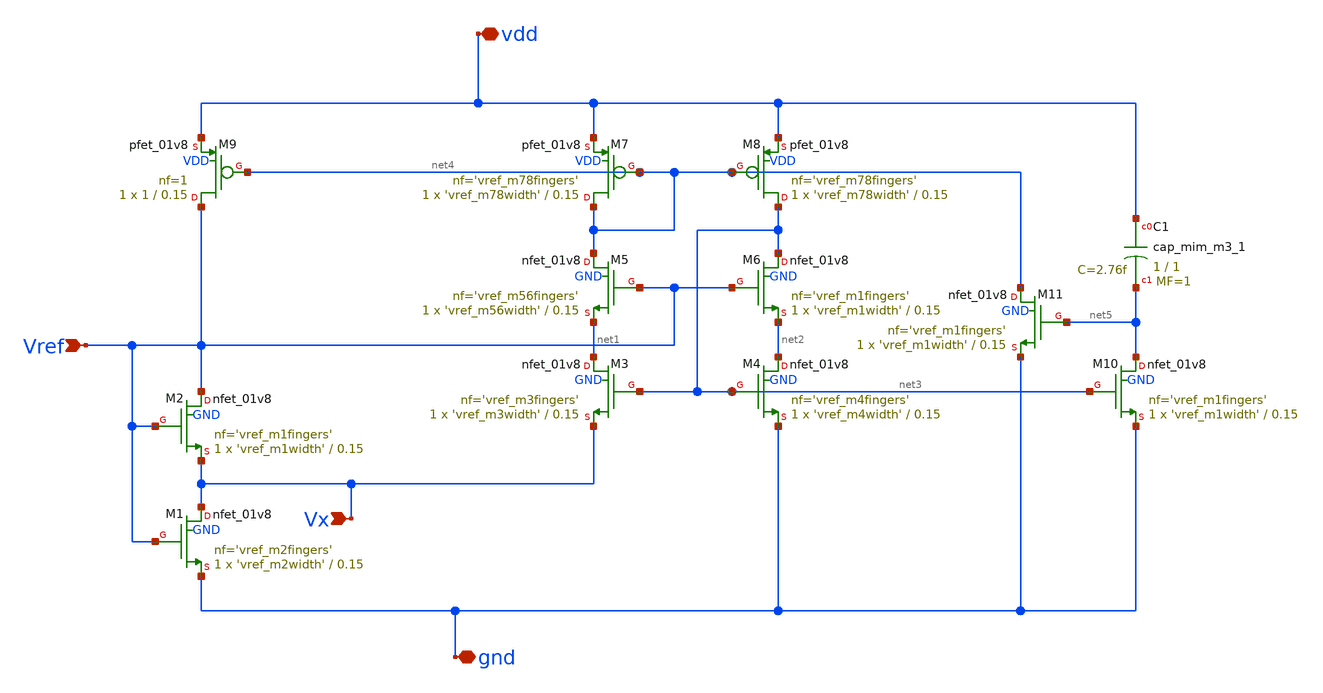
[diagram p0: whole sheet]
** sch_path: xschem/cmos_vref.sch
**.subckt cmos_vref Vref gnd vdd Vx
*.ipin Vref
*.iopin gnd
*.iopin vdd
*.ipin Vx
XM2 Vref Vref Vx GND sky130_fd_pr__nfet_01v8 L=0.15 W='vref_m1width' nf='vref_m1fingers' ad='int((nf+1)/2) * W/nf * 0.29'
+ as='int((nf+2)/2) * W/nf * 0.29' pd='2*int((nf+1)/2) * (W/nf + 0.29)' ps='2*int((nf+2)/2) * (W/nf + 0.29)'
+ nrd='0.29 / W' nrs='0.29 / W' sa=0 sb=0 sd=0 mult=1 m=1
XM1 Vx Vref gnd GND sky130_fd_pr__nfet_01v8 L=0.15 W='vref_m2width' nf='vref_m2fingers' ad='int((nf+1)/2) * W/nf * 0.29'
+ as='int((nf+2)/2) * W/nf * 0.29' pd='2*int((nf+1)/2) * (W/nf + 0.29)' ps='2*int((nf+2)/2) * (W/nf + 0.29)'
+ nrd='0.29 / W' nrs='0.29 / W' sa=0 sb=0 sd=0 mult=1 m=1
XM3 net1 net3 Vx GND sky130_fd_pr__nfet_01v8 L=0.15 W='vref_m3width' nf='vref_m3fingers' ad='int((nf+1)/2) * W/nf * 0.29'
+ as='int((nf+2)/2) * W/nf * 0.29' pd='2*int((nf+1)/2) * (W/nf + 0.29)' ps='2*int((nf+2)/2) * (W/nf + 0.29)'
+ nrd='0.29 / W' nrs='0.29 / W' sa=0 sb=0 sd=0 mult=1 m=1
XM4 net2 net3 gnd GND sky130_fd_pr__nfet_01v8 L=0.15 W='vref_m4width' nf='vref_m4fingers' ad='int((nf+1)/2) * W/nf * 0.29'
+ as='int((nf+2)/2) * W/nf * 0.29' pd='2*int((nf+1)/2) * (W/nf + 0.29)' ps='2*int((nf+2)/2) * (W/nf + 0.29)'
+ nrd='0.29 / W' nrs='0.29 / W' sa=0 sb=0 sd=0 mult=1 m=1
XM5 net4 Vref net1 GND sky130_fd_pr__nfet_01v8 L=0.15 W='vref_m56width' nf='vref_m56fingers' ad='int((nf+1)/2) * W/nf * 0.29'
+ as='int((nf+2)/2) * W/nf * 0.29' pd='2*int((nf+1)/2) * (W/nf + 0.29)' ps='2*int((nf+2)/2) * (W/nf + 0.29)'
+ nrd='0.29 / W' nrs='0.29 / W' sa=0 sb=0 sd=0 mult=1 m=1
XM6 net3 Vref net2 GND sky130_fd_pr__nfet_01v8 L=0.15 W='vref_m1width' nf='vref_m1fingers' ad='int((nf+1)/2) * W/nf * 0.29'
+ as='int((nf+2)/2) * W/nf * 0.29' pd='2*int((nf+1)/2) * (W/nf + 0.29)' ps='2*int((nf+2)/2) * (W/nf + 0.29)'
+ nrd='0.29 / W' nrs='0.29 / W' sa=0 sb=0 sd=0 mult=1 m=1
XM7 net4 net4 vdd VDD sky130_fd_pr__pfet_01v8 L=0.15 W='vref_m78width' nf='vref_m78fingers' ad='int((nf+1)/2) * W/nf * 0.29'
+ as='int((nf+2)/2) * W/nf * 0.29' pd='2*int((nf+1)/2) * (W/nf + 0.29)' ps='2*int((nf+2)/2) * (W/nf + 0.29)'
+ nrd='0.29 / W' nrs='0.29 / W' sa=0 sb=0 sd=0 mult=1 m=1
XM8 net3 net4 vdd VDD sky130_fd_pr__pfet_01v8 L=0.15 W='vref_m78width' nf='vref_m78fingers' ad='int((nf+1)/2) * W/nf * 0.29'
+ as='int((nf+2)/2) * W/nf * 0.29' pd='2*int((nf+1)/2) * (W/nf + 0.29)' ps='2*int((nf+2)/2) * (W/nf + 0.29)'
+ nrd='0.29 / W' nrs='0.29 / W' sa=0 sb=0 sd=0 mult=1 m=1
XM9 Vref net4 vdd VDD sky130_fd_pr__pfet_01v8 L=0.15 W=1 nf=1 ad='int((nf+1)/2) * W/nf * 0.29' as='int((nf+2)/2) * W/nf * 0.29'
+ pd='2*int((nf+1)/2) * (W/nf + 0.29)' ps='2*int((nf+2)/2) * (W/nf + 0.29)' nrd='0.29 / W' nrs='0.29 / W'
+ sa=0 sb=0 sd=0 mult=1 m=1
XM10 net5 net3 gnd GND sky130_fd_pr__nfet_01v8 L=0.15 W='vref_m1width' nf='vref_m1fingers' ad='int((nf+1)/2) * W/nf * 0.29'
+ as='int((nf+2)/2) * W/nf * 0.29' pd='2*int((nf+1)/2) * (W/nf + 0.29)' ps='2*int((nf+2)/2) * (W/nf + 0.29)'
+ nrd='0.29 / W' nrs='0.29 / W' sa=0 sb=0 sd=0 mult=1 m=1
XM11 net4 net5 gnd GND sky130_fd_pr__nfet_01v8 L=0.15 W='vref_m1width' nf='vref_m1fingers' ad='int((nf+1)/2) * W/nf * 0.29'
+ as='int((nf+2)/2) * W/nf * 0.29' pd='2*int((nf+1)/2) * (W/nf + 0.29)' ps='2*int((nf+2)/2) * (W/nf + 0.29)'
+ nrd='0.29 / W' nrs='0.29 / W' sa=0 sb=0 sd=0 mult=1 m=1
XC1 vdd net5 sky130_fd_pr__cap_mim_m3_1 W=1 L=1 MF=1 m=1
**.ends
.end
